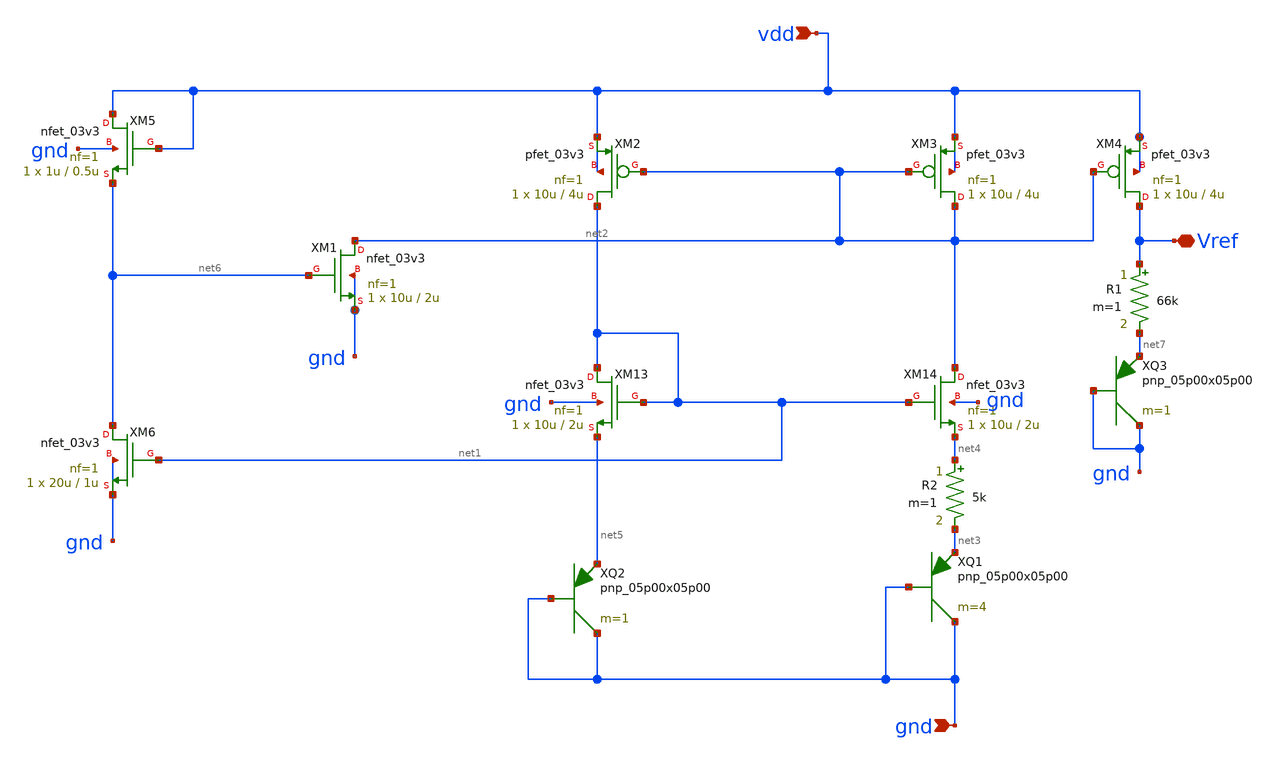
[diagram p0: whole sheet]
** sch_path: xschem/bias_generator/BGR_BJT.sch
**.subckt BGR_BJT gnd Vref vdd
*.ipin gnd
*.iopin Vref
*.ipin vdd
XM2 net1 net2 vdd vdd pfet_03v3 L=4u W=10u nf=1 ad='int((nf+1)/2) * W/nf * 0.18u' as='int((nf+2)/2) * W/nf * 0.18u'
+ pd='2*int((nf+1)/2) * (W/nf + 0.18u)' ps='2*int((nf+2)/2) * (W/nf + 0.18u)' nrd='0.18u / W' nrs='0.18u / W'
+ sa=0 sb=0 sd=0 m=1
XM3 net2 net2 vdd vdd pfet_03v3 L=4u W=10u nf=1 ad='int((nf+1)/2) * W/nf * 0.18u' as='int((nf+2)/2) * W/nf * 0.18u'
+ pd='2*int((nf+1)/2) * (W/nf + 0.18u)' ps='2*int((nf+2)/2) * (W/nf + 0.18u)' nrd='0.18u / W' nrs='0.18u / W'
+ sa=0 sb=0 sd=0 m=1
XM4 Vref net2 vdd vdd pfet_03v3 L=4u W=10u nf=1 ad='int((nf+1)/2) * W/nf * 0.18u' as='int((nf+2)/2) * W/nf * 0.18u'
+ pd='2*int((nf+1)/2) * (W/nf + 0.18u)' ps='2*int((nf+2)/2) * (W/nf + 0.18u)' nrd='0.18u / W' nrs='0.18u / W'
+ sa=0 sb=0 sd=0 m=1
XM13 net1 net1 net5 gnd nfet_03v3 L=2u W=10u nf=1 ad='int((nf+1)/2) * W/nf * 0.18u' as='int((nf+2)/2) * W/nf * 0.18u'
+ pd='2*int((nf+1)/2) * (W/nf + 0.18u)' ps='2*int((nf+2)/2) * (W/nf + 0.18u)' nrd='0.18u / W' nrs='0.18u / W'
+ sa=0 sb=0 sd=0 m=1
XM14 net2 net1 net4 gnd nfet_03v3 L=2u W=10u nf=1 ad='int((nf+1)/2) * W/nf * 0.18u' as='int((nf+2)/2) * W/nf * 0.18u'
+ pd='2*int((nf+1)/2) * (W/nf + 0.18u)' ps='2*int((nf+2)/2) * (W/nf + 0.18u)' nrd='0.18u / W' nrs='0.18u / W'
+ sa=0 sb=0 sd=0 m=1
R1 Vref net7 66k m=1
R2 net4 net3 5k m=1
XQ1 gnd gnd net3 pnp_05p00x05p00 m=4 par=4
XQ2 gnd gnd net5 pnp_05p00x05p00 m=1 par=1
XM1 net2 net6 gnd gnd nfet_03v3 L=2u W=10u nf=1 ad='int((nf+1)/2) * W/nf * 0.18u' as='int((nf+2)/2) * W/nf * 0.18u'
+ pd='2*int((nf+1)/2) * (W/nf + 0.18u)' ps='2*int((nf+2)/2) * (W/nf + 0.18u)' nrd='0.18u / W' nrs='0.18u / W'
+ sa=0 sb=0 sd=0 m=1
XM5 vdd vdd net6 gnd nfet_03v3 L=0.5u W=1u nf=1 ad='int((nf+1)/2) * W/nf * 0.18u' as='int((nf+2)/2) * W/nf * 0.18u'
+ pd='2*int((nf+1)/2) * (W/nf + 0.18u)' ps='2*int((nf+2)/2) * (W/nf + 0.18u)' nrd='0.18u / W' nrs='0.18u / W'
+ sa=0 sb=0 sd=0 m=1
XM6 net6 net1 gnd gnd nfet_03v3 L=1u W=20u nf=1 ad='int((nf+1)/2) * W/nf * 0.18u' as='int((nf+2)/2) * W/nf * 0.18u'
+ pd='2*int((nf+1)/2) * (W/nf + 0.18u)' ps='2*int((nf+2)/2) * (W/nf + 0.18u)' nrd='0.18u / W' nrs='0.18u / W'
+ sa=0 sb=0 sd=0 m=1
XQ3 gnd gnd net7 pnp_05p00x05p00 m=1 par=1
**.ends
.end
